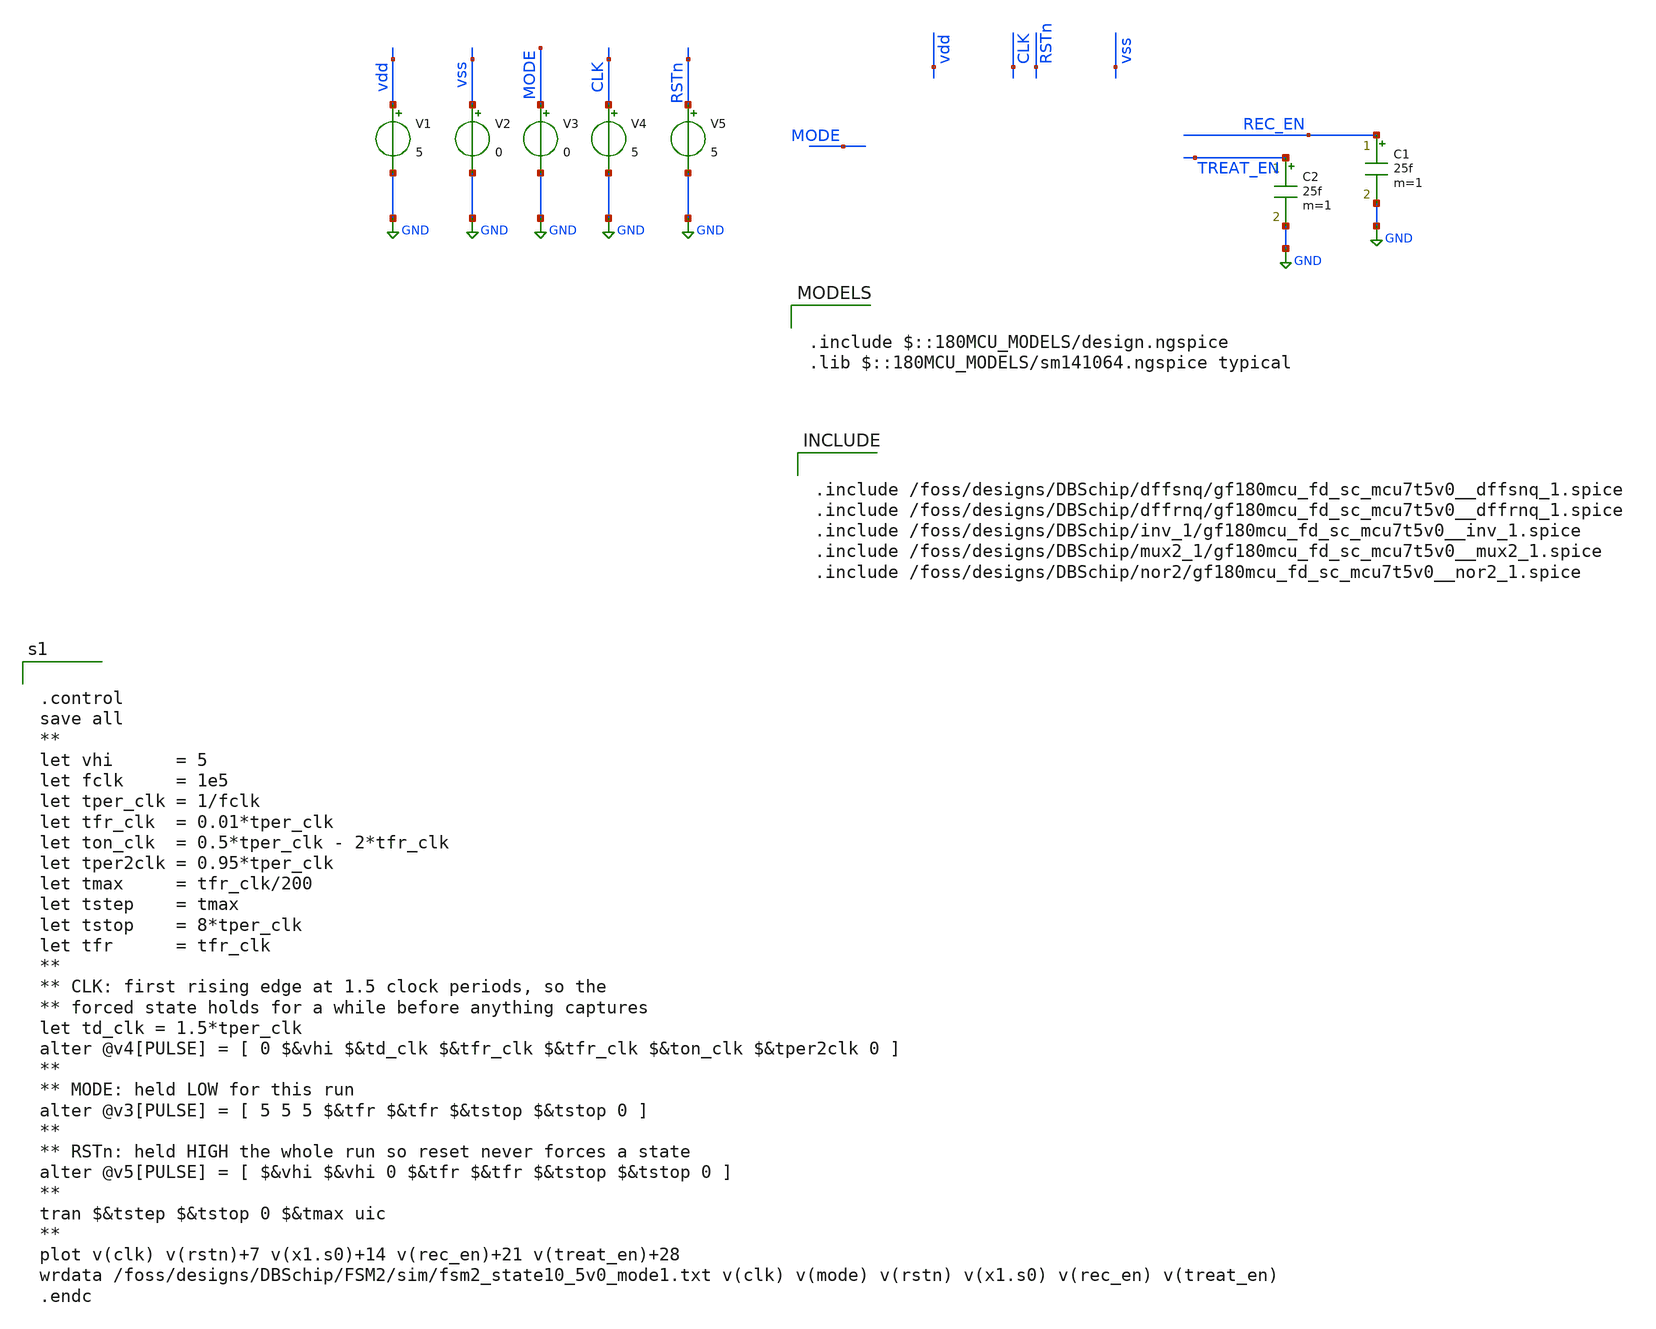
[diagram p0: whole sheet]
** sch_path: FSM2/FSM2_tb_postPEX.sch
**.subckt FSM2_tb_postPEX
V1 vdd GND 5
V2 vss GND 0
V3 MODE GND 0
V4 CLK GND 5
V5 RSTn GND 5
C1 REC_EN GND 25f m=1
C2 TREAT_EN GND 25f m=1
**** begin user architecture code

.include $::180MCU_MODELS/design.ngspice
.lib $::180MCU_MODELS/sm141064.ngspice typical



.include /foss/designs/DBSchip/dffsnq/gf180mcu_fd_sc_mcu7t5v0__dffsnq_1.spice
.include /foss/designs/DBSchip/dffrnq/gf180mcu_fd_sc_mcu7t5v0__dffrnq_1.spice
.include /foss/designs/DBSchip/inv_1/gf180mcu_fd_sc_mcu7t5v0__inv_1.spice
.include /foss/designs/DBSchip/mux2_1/gf180mcu_fd_sc_mcu7t5v0__mux2_1.spice
.include /foss/designs/DBSchip/nor2/gf180mcu_fd_sc_mcu7t5v0__nor2_1.spice




* NGSPICE file created from FSM2.ext - technology: gf180mcuD

.subckt dffsnq SETN Q CLK VNW VPW a_1836_282# a_855_238# a_1492_238# a_3220_277# a_1179_653#
+  a_975_282# a_175_277# a_587_598# a_383_277# a_1432_653# a_2588_282# a_2364_282#  a_3268_233# a_383_598#
+ a_1423_282#
X0 a_975_282# a_855_238# a_383_598# VNW pfet_05v0 ad=0.1313p pd=1.025u as=0.22725p ps=1.91u w=0.505u
+ l=0.5u
X1 a_383_598# a_1492_238# a_1432_653# VNW pfet_05v0 ad=0.3975p pd=2.185u as=0.101p ps=0.905u
+ w=0.505u l=0.5u
X2 a_1836_282# a_1179_653# a_383_277# VPW nfet_05v0 ad=86.39999f pd=0.84u as=93.59999f ps=0.88u
+ w=0.36u l=0.6u
X3 a_587_598# a_175_277# a_383_598# VNW pfet_05v0 ad=0.3806p pd=2.61u as=0.2249p ps=1.385u w=0.865u
+ l=0.5u
X4 a_1432_653# a_175_277# a_1179_653# VNW pfet_05v0 ad=0.101p pd=0.905u as=0.19315p ps=1.27u
+ w=0.505u l=0.5u
X5 a_2364_282# a_175_277# a_1492_238# VNW pfet_05v0 ad=0.1079p pd=0.935u as=0.27805p ps=2.17u
+ w=0.415u l=0.5u
X6 a_2588_282# SETN a_383_598# VNW pfet_05v0 ad=0.2028p pd=1.3u as=0.3432p ps=2.44u w=0.78u l=0.5u
X7 a_1179_653# a_175_277# a_975_282# VPW nfet_05v0 ad=93.59999f pd=0.88u as=93.59999f ps=0.88u
+ w=0.36u l=0.6u
X8 a_383_277# a_3268_233# a_3220_277# VPW nfet_05v0 ad=0.14985p pd=1.145u as=48.6f ps=0.645u
+ w=0.405u l=0.6u
X9 a_383_277# a_1492_238# a_1423_282# VPW nfet_05v0 ad=93.59999f pd=0.88u as=62.1f ps=0.705u w=0.36u
+ l=0.6u
X10 a_2364_282# a_587_598# a_1492_238# VPW nfet_05v0 ad=93.59999f pd=0.88u as=0.1989p ps=1.465u
+ w=0.36u l=0.6u
X11 a_1179_653# a_587_598# a_975_282# VNW pfet_05v0 ad=0.19315p pd=1.27u as=0.1313p ps=1.025u
+ w=0.505u l=0.5u
X12 a_587_598# a_175_277# a_383_277# VPW nfet_05v0 ad=0.1782p pd=1.69u as=0.1053p ps=0.925u w=0.405u
+ l=0.6u
X13 a_1492_238# SETN a_1836_282# VPW nfet_05v0 ad=0.1989p pd=1.465u as=86.39999f ps=0.84u w=0.36u
+ l=0.6u
X14 a_2588_282# a_587_598# a_2364_282# VNW pfet_05v0 ad=0.1826p pd=1.71u as=0.1079p ps=0.935u
+ w=0.415u l=0.5u
X15 a_383_598# a_3268_233# a_2588_282# VNW pfet_05v0 ad=0.3276p pd=1.62u as=0.2028p ps=1.3u w=0.78u
+ l=0.5u
X16 a_975_282# a_855_238# a_383_277# VPW nfet_05v0 ad=93.59999f pd=0.88u as=0.1584p ps=1.6u w=0.36u
+ l=0.6u
X17 a_3220_277# SETN a_2588_282# VPW nfet_05v0 ad=48.6f pd=0.645u as=0.3123p ps=2.38u w=0.405u
+ l=0.6u
X18 a_383_277# CLK a_175_277# VPW nfet_05v0 ad=0.1053p pd=0.925u as=0.1782p ps=1.69u w=0.405u l=0.6u
X19 a_3268_233# a_2364_282# a_383_277# VPW nfet_05v0 ad=0.1782p pd=1.69u as=0.14985p ps=1.145u
+ w=0.405u l=0.6u
X20 Q a_3268_233# a_383_598# VNW pfet_05v0 ad=0.6561p pd=3.51u as=0.5346p ps=3.31u w=1.215u l=0.5u
X21 a_383_598# SETN a_1492_238# VNW pfet_05v0 ad=0.4149p pd=2.65u as=0.1521p ps=1.105u w=0.585u
+ l=0.5u
X22 a_2588_282# a_175_277# a_2364_282# VPW nfet_05v0 ad=0.2898p pd=2.33u as=93.59999f ps=0.88u
+ w=0.36u l=0.6u
X23 a_3268_233# a_2364_282# a_383_598# VNW pfet_05v0 ad=0.3432p pd=2.44u as=0.3276p ps=1.62u w=0.78u
+ l=0.5u
X24 a_1492_238# a_1179_653# a_383_598# VNW pfet_05v0 ad=0.1521p pd=1.105u as=0.3975p ps=2.185u
+ w=0.585u l=0.5u
X25 Q a_3268_233# a_383_277# VPW nfet_05v0 ad=0.3586p pd=2.51u as=0.3586p ps=2.51u w=0.815u l=0.6u
X26 a_383_598# CLK a_175_277# VNW pfet_05v0 ad=0.2249p pd=1.385u as=0.3806p ps=2.61u w=0.865u l=0.5u
X27 a_1423_282# a_587_598# a_1179_653# VPW nfet_05v0 ad=62.1f pd=0.705u as=93.59999f ps=0.88u
+ w=0.36u l=0.6u
C0 a_383_277# a_175_277# 0.28633f
C1 a_1432_653# a_1179_653# 0.00215f
C2 SETN VNW 0.81105f
C3 a_975_282# a_175_277# 0.0157f
C4 a_3220_277# a_2364_282# 0.00413f
C5 a_383_277# a_383_598# 0.01381f
C6 a_1432_653# a_1492_238# 0
C7 SETN a_3268_233# 0.08929f
C8 a_1179_653# a_175_277# 0.20639f
C9 a_1179_653# a_383_598# 0.03968f
C10 a_175_277# a_1492_238# 0.84088f
C11 a_383_277# a_975_282# 0.05001f
C12 a_1836_282# a_1492_238# 0.00275f
C13 a_383_598# a_1492_238# 0.01626f
C14 Q a_175_277# 0
C15 a_383_277# a_1179_653# 0.06022f
C16 a_975_282# a_1179_653# 0.06821f
C17 Q a_383_598# 0.28218f
C18 a_587_598# a_855_238# 0.4001f
C19 a_383_277# a_1492_238# 0.02735f
C20 a_2588_282# a_587_598# 0.05668f
C21 VNW a_855_238# 0.1615f
C22 VNW a_2588_282# 0.04382f
C23 a_383_277# Q 0.13127f
C24 a_1423_282# a_587_598# 0.00269f
C25 VNW a_587_598# 0.40096f
C26 a_1179_653# a_1492_238# 0.38742f
C27 a_3268_233# a_2588_282# 0.00955f
C28 a_2364_282# a_175_277# 0.15368f
C29 a_3268_233# a_587_598# 0
C30 a_2364_282# a_383_598# 0.07341f
C31 a_3220_277# a_2588_282# 0.0012f
C32 a_3268_233# VNW 0.32346f
C33 SETN a_175_277# 0.07777f
C34 a_383_277# a_2364_282# 1.18908f
C35 SETN a_383_598# 0.12782f
C36 SETN a_383_277# 0.00808f
C37 a_2364_282# a_1492_238# 0.15287f
C38 CLK a_587_598# 0.00131f
C39 a_2364_282# Q 0
C40 CLK VNW 0.13659f
C41 SETN a_1179_653# 0.06324f
C42 SETN a_1492_238# 0.07298f
C43 a_175_277# a_855_238# 0.0927f
C44 a_2588_282# a_175_277# 0.00597f
C45 a_383_598# a_855_238# 0.00494f
C46 a_175_277# a_587_598# 0.47313f
C47 a_2588_282# a_383_598# 0.20863f
C48 a_1836_282# a_587_598# 0.00762f
C49 VNW a_175_277# 0.90944f
C50 a_383_598# a_587_598# 0.62458f
C51 a_383_277# a_855_238# 0.06788f
C52 a_975_282# a_855_238# 0.1081f
C53 VNW a_383_598# 0.5391f
C54 a_3268_233# a_175_277# 0
C55 a_383_277# a_587_598# 1.07431f
C56 a_383_277# a_1423_282# 0.00364f
C57 a_975_282# a_587_598# 0.42776f
C58 a_1179_653# a_855_238# 0
C59 a_3268_233# a_383_598# 0.35131f
C60 a_383_277# VNW 0.00946f
C61 SETN a_2364_282# 0.0706f
C62 a_975_282# VNW 0.01368f
C63 a_3220_277# a_383_598# 0
C64 a_1179_653# a_587_598# 0.86961f
C65 a_2588_282# a_1492_238# 0
C66 a_1179_653# a_1423_282# 0
C67 a_383_277# a_3268_233# 0.13677f
C68 a_1179_653# VNW 0.22386f
C69 a_587_598# a_1492_238# 0.31725f
C70 VNW a_1492_238# 0.21951f
C71 Q a_587_598# 0
C72 Q VNW 0.03162f
C73 CLK a_175_277# 0.70097f
C74 CLK a_383_598# 0.02209f
C75 a_3268_233# Q 0.17947f
C76 a_1432_653# a_175_277# 0.00838f
C77 a_2364_282# a_2588_282# 0.56917f
C78 a_383_277# CLK 0.02194f
C79 a_2364_282# a_587_598# 0.154f
C80 a_2364_282# VNW 0.20903f
C81 a_383_598# a_175_277# 1.41468f
C82 SETN a_2588_282# 0.30222f
C83 a_3268_233# a_2364_282# 0.51404f
C84 SETN a_587_598# 0.0839f
C85 Q VPW 0.10557f
C86 SETN VPW 0.71025f
C87 CLK VPW 0.29047f
C88 VNW VPW 6.44257f
C89 a_2588_282# VPW 0.04999f
C90 a_383_277# VPW 1.35707f
C91 a_2364_282# VPW 0.43408f
C92 a_3268_233# VPW 0.58406f
C93 a_975_282# VPW 0.01977f
C94 a_1179_653# VPW 0.30208f
C95 a_1492_238# VPW 0.28651f
C96 a_855_238# VPW 0.2471f
C97 a_587_598# VPW 1.21246f
C98 a_383_598# VPW 0.83318f
C99 a_175_277# VPW 1.31409f
.ends

.subckt or2 MODE A1 VNW VPW a_n505_n1653# a_159_n1784# a_n525_n2163# a_n317_n1653#  a_n113_n1653#
X0 a_159_n1784# a_n505_n1653# a_n113_n1653# VNW pfet_05v0 ad=0.5368p pd=3.32u as=0.38705p ps=2.08u
+ w=1.22u l=0.5u
X1 a_n317_n1653# A1 a_n505_n1653# VNW pfet_05v0 ad=0.1469p pd=1.085u as=0.2486p ps=2.01u w=0.565u
+ l=0.5u
X2 a_159_n1784# a_n505_n1653# a_n525_n2163# VPW nfet_05v0 ad=0.3608p pd=2.52u as=0.2288p ps=1.58u
+ w=0.82u l=0.6u
X3 a_n113_n1653# MODE a_n317_n1653# VNW pfet_05v0 ad=0.38705p pd=2.08u as=0.1469p ps=1.085u w=0.565u
+ l=0.5u
X4 a_n525_n2163# MODE a_n505_n1653# VPW nfet_05v0 ad=0.2288p pd=1.58u as=93.59999f ps=0.88u w=0.36u
+ l=0.6u
X5 a_n505_n1653# A1 a_n525_n2163# VPW nfet_05v0 ad=93.59999f pd=0.88u as=0.1584p ps=1.6u w=0.36u
+ l=0.6u
C0 a_n525_n2163# VNW 0.01004f
C1 a_n317_n1653# a_n113_n1653# 0.00536f
C2 VNW MODE 0.21631f
C3 a_n505_n1653# VNW 0.15724f
C4 a_n525_n2163# a_n113_n1653# 0.00865f
C5 a_n113_n1653# MODE 0.14763f
C6 a_n505_n1653# a_n113_n1653# 0.30704f
C7 a_n525_n2163# A1 0.05074f
C8 a_n525_n2163# a_159_n1784# 0.15826f
C9 VNW a_n113_n1653# 0.11771f
C10 a_n317_n1653# a_n525_n2163# 0
C11 A1 MODE 0.0624f
C12 a_159_n1784# MODE 0.0276f
C13 a_n505_n1653# A1 0.54089f
C14 a_n505_n1653# a_159_n1784# 0.18159f
C15 a_n317_n1653# MODE 0.00196f
C16 a_n317_n1653# a_n505_n1653# 0.00762f
C17 VNW A1 0.22f
C18 VNW a_159_n1784# 0.03388f
C19 a_n525_n2163# MODE 0.02575f
C20 a_n525_n2163# a_n505_n1653# 0.25049f
C21 a_n505_n1653# MODE 0.50537f
C22 a_n113_n1653# A1 0.01431f
C23 a_n113_n1653# a_159_n1784# 0.19605f
C24 MODE VPW 0.31344f
C25 A1 VPW 0.39469f
C26 VNW VPW 1.65967f
C27 a_n525_n2163# VPW 0.35972f
C28 a_159_n1784# VPW 0.10275f
C29 a_n113_n1653# VPW 0.23302f
C30 a_n505_n1653# VPW 0.34568f
.ends

.subckt nor2 REC_EN TREAT_EN A2 VSS VDD w_1180_n1958# a_1490_n1804# VSUBS
X0 a_1490_n1804# REC_EN VDD w_1180_n1958# pfet_05v0 ad=0.4087p pd=1.89u as=0.5368p ps=3.32u w=1.22u
+ l=0.5u
X1 TREAT_EN REC_EN VSS VSUBS nfet_05v0 ad=0.1469p pd=1.085u as=0.2486p ps=2.01u w=0.565u l=0.6u
X2 TREAT_EN A2 a_1490_n1804# w_1180_n1958# pfet_05v0 ad=0.5368p pd=3.32u as=0.4087p ps=1.89u w=1.22u
+ l=0.5u
X3 VSS A2 TREAT_EN VSUBS nfet_05v0 ad=0.2486p pd=2.01u as=0.1469p ps=1.085u w=0.565u l=0.6u
C0 TREAT_EN w_1180_n1958# 0.01978f
C1 A2 w_1180_n1958# 0.13314f
C2 w_1180_n1958# REC_EN 0.1288f
C3 TREAT_EN A2 0.57853f
C4 VDD w_1180_n1958# 0.09421f
C5 TREAT_EN REC_EN 0.37841f
C6 A2 REC_EN 0.03781f
C7 TREAT_EN VDD 0.11792f
C8 A2 VDD 0.0227f
C9 VSS a_1490_n1804# 0
C10 VDD REC_EN 0.25532f
C11 VSS w_1180_n1958# 0.01214f
C12 TREAT_EN a_1490_n1804# 0.02369f
C13 TREAT_EN VSS 0.08738f
C14 A2 VSS 0.16225f
C15 a_1490_n1804# REC_EN 0.00898f
C16 VDD a_1490_n1804# 0.01396f
C17 VSS REC_EN 0.04452f
C18 VSS VDD 0.02591f
C19 VDD VSUBS 0.21903f
C20 TREAT_EN VSUBS 0.05889f
C21 VSS VSUBS 0.3776f
C22 A2 VSUBS 0.32864f
C23 REC_EN VSUBS 0.33451f
C24 w_1180_n1958# VSUBS 1.31158f
.ends

.subckt dffrnq RN Q CLK VNW VPW a_1002_n2102# a_1458_n1702# a_2250_n1702# a_2667_n1842#  a_38_n1706#
+ a_798_n2102# a_698_n2146# a_450_n2119# a_1310_n2146# a_246_n2119# a_246_n1706#  a_1206_n2102# a_1290_n1702#
+ a_2562_n1702# a_3043_n1702#
X0 a_246_n1706# RN a_1458_n1702# VPW nfet_05v0 ad=0.2016p pd=1.48u as=43.2f ps=0.6u w=0.36u l=0.6u
X1 a_3043_n1702# RN a_246_n1706# VPW nfet_05v0 ad=0.134p pd=1.1u as=0.1224p ps=1.04u w=0.36u l=0.6u
X2 a_2562_n1702# a_450_n2119# a_2250_n1702# VNW pfet_05v0 ad=0.1313p pd=1.025u as=0.25375p ps=1.51u
+ w=0.505u l=0.5u
X3 a_798_n2102# a_698_n2146# a_246_n2119# VNW pfet_05v0 ad=0.2028p pd=1.3u as=0.3432p ps=2.44u
+ w=0.78u l=0.5u
X4 a_246_n1706# a_2667_n1842# a_2562_n1702# VPW nfet_05v0 ad=0.1224p pd=1.04u as=94.5f ps=0.885u
+ w=0.36u l=0.6u
X5 a_450_n2119# a_38_n1706# a_246_n1706# VPW nfet_05v0 ad=0.1782p pd=1.69u as=0.1053p ps=0.925u
+ w=0.405u l=0.6u
X6 a_1206_n2102# a_38_n1706# a_1002_n2102# VNW pfet_05v0 ad=0.2028p pd=1.3u as=0.2028p ps=1.3u
+ w=0.78u l=0.5u
X7 a_2667_n1842# a_2250_n1702# a_3043_n1702# VPW nfet_05v0 ad=0.176p pd=1.68u as=0.134p ps=1.1u
+ w=0.4u l=0.6u
X8 a_1206_n2102# RN a_246_n2119# VNW pfet_05v0 ad=0.3432p pd=2.44u as=0.45p ps=2.02u w=0.78u l=0.5u
X9 a_2562_n1702# a_38_n1706# a_2250_n1702# VPW nfet_05v0 ad=94.5f pd=0.885u as=0.2007p ps=1.475u
+ w=0.36u l=0.6u
X10 a_246_n1706# CLK a_38_n1706# VPW nfet_05v0 ad=0.1053p pd=0.925u as=0.1782p ps=1.69u w=0.405u
+ l=0.6u
X11 a_1310_n2146# a_1002_n2102# a_246_n2119# VNW pfet_05v0 ad=0.2424p pd=1.465u as=0.2222p ps=1.89u
+ w=0.505u l=0.5u
X12 a_2667_n1842# RN a_246_n2119# VNW pfet_05v0 ad=0.26p pd=1.52u as=0.29465p ps=1.74u w=1u l=0.5u
X13 a_2250_n1702# a_450_n2119# a_1310_n2146# VPW nfet_05v0 ad=0.2007p pd=1.475u as=0.2007p ps=1.475u
+ w=0.36u l=0.6u
X14 a_246_n2119# CLK a_38_n1706# VNW pfet_05v0 ad=0.2249p pd=1.385u as=0.3806p ps=2.61u w=0.865u
+ l=0.5u
X15 a_246_n2119# a_2667_n1842# a_2562_n1702# VNW pfet_05v0 ad=0.29465p pd=1.74u as=0.1313p ps=1.025u
+ w=0.505u l=0.5u
X16 a_1290_n1702# a_450_n2119# a_1002_n2102# VPW nfet_05v0 ad=43.2f pd=0.6u as=93.59999f ps=0.88u
+ w=0.36u l=0.6u
X17 Q a_2667_n1842# a_246_n2119# VNW pfet_05v0 ad=0.63787p pd=3.48u as=0.5346p ps=3.31u w=1.215u
+ l=0.5u
X18 a_246_n2119# a_1310_n2146# a_1206_n2102# VNW pfet_05v0 ad=0.45p pd=2.02u as=0.2028p ps=1.3u
+ w=0.78u l=0.5u
X19 Q a_2667_n1842# a_246_n1706# VPW nfet_05v0 ad=0.42787p pd=2.68u as=0.3586p ps=2.51u w=0.815u
+ l=0.6u
X20 a_798_n2102# a_698_n2146# a_246_n1706# VPW nfet_05v0 ad=93.59999f pd=0.88u as=0.1584p ps=1.6u
+ w=0.36u l=0.6u
X21 a_2250_n1702# a_38_n1706# a_1310_n2146# VNW pfet_05v0 ad=0.25375p pd=1.51u as=0.2424p ps=1.465u
+ w=0.505u l=0.5u
X22 a_246_n2119# a_2250_n1702# a_2667_n1842# VNW pfet_05v0 ad=0.44p pd=2.88u as=0.26p ps=1.52u w=1u
+ l=0.5u
X23 a_1002_n2102# a_38_n1706# a_798_n2102# VPW nfet_05v0 ad=93.59999f pd=0.88u as=93.59999f ps=0.88u
+ w=0.36u l=0.6u
X24 a_450_n2119# a_38_n1706# a_246_n2119# VNW pfet_05v0 ad=0.3806p pd=2.61u as=0.2249p ps=1.385u
+ w=0.865u l=0.5u
X25 a_1002_n2102# a_450_n2119# a_798_n2102# VNW pfet_05v0 ad=0.2028p pd=1.3u as=0.2028p ps=1.3u
+ w=0.78u l=0.5u
X26 a_1458_n1702# a_1310_n2146# a_1290_n1702# VPW nfet_05v0 ad=43.2f pd=0.6u as=43.2f ps=0.6u
+ w=0.36u l=0.6u
X27 a_1310_n2146# a_1002_n2102# a_246_n1706# VPW nfet_05v0 ad=0.2007p pd=1.475u as=0.2016p ps=1.48u
+ w=0.36u l=0.6u
C0 a_38_n1706# a_2667_n1842# 0.01904f
C1 RN a_246_n2119# 0.03498f
C2 a_246_n1706# Q 0.11398f
C3 a_1002_n2102# a_798_n2102# 0.04844f
C4 a_2562_n1702# a_2667_n1842# 0.11606f
C5 a_1310_n2146# a_246_n2119# 0.09419f
C6 a_38_n1706# a_450_n2119# 0.53697f
C7 a_2562_n1702# a_450_n2119# 0.27749f
C8 VNW CLK 0.13704f
C9 a_1002_n2102# a_246_n2119# 0.11921f
C10 a_1002_n2102# a_1290_n1702# 0
C11 a_2667_n1842# a_3043_n1702# 0.00177f
C12 a_38_n1706# a_2562_n1702# 0.00367f
C13 a_1002_n2102# a_698_n2146# 0
C14 VNW Q 0.03166f
C15 a_246_n1706# a_2667_n1842# 0.18639f
C16 RN Q 0
C17 a_450_n2119# a_246_n1706# 1.20327f
C18 a_450_n2119# a_1206_n2102# 0.009f
C19 a_38_n1706# a_246_n1706# 0.29961f
C20 a_2562_n1702# a_246_n1706# 0.1285f
C21 VNW a_2667_n1842# 0.35472f
C22 a_450_n2119# VNW 0.34128f
C23 a_38_n1706# a_1206_n2102# 0.007f
C24 RN a_2667_n1842# 0.33647f
C25 a_246_n2119# a_2250_n1702# 1.11667f
C26 a_450_n2119# RN 0.07873f
C27 a_246_n2119# a_798_n2102# 0
C28 a_450_n2119# a_1310_n2146# 0.8821f
C29 a_38_n1706# VNW 1.28833f
C30 a_2562_n1702# VNW 0.02016f
C31 a_698_n2146# a_798_n2102# 0.08286f
C32 a_1002_n2102# a_450_n2119# 0.36196f
C33 a_38_n1706# RN 0.0801f
C34 a_38_n1706# a_1310_n2146# 0.05539f
C35 a_2562_n1702# RN 0.03878f
C36 a_698_n2146# a_246_n2119# 0.00937f
C37 a_1002_n2102# a_38_n1706# 0.08126f
C38 Q a_2250_n1702# 0.01436f
C39 VNW a_246_n1706# 0.0106f
C40 RN a_3043_n1702# 0.01068f
C41 CLK a_246_n2119# 0.02303f
C42 VNW a_1206_n2102# 0.01627f
C43 RN a_246_n1706# 0.45994f
C44 Q a_246_n2119# 0.1499f
C45 a_246_n1706# a_1310_n2146# 0.01482f
C46 RN a_1206_n2102# 0.02104f
C47 a_1002_n2102# a_246_n1706# 0.04356f
C48 a_1206_n2102# a_1310_n2146# 0.02667f
C49 a_2667_n1842# a_2250_n1702# 0.63332f
C50 a_450_n2119# a_2250_n1702# 0.51037f
C51 a_450_n2119# a_1458_n1702# 0.00227f
C52 RN VNW 0.32949f
C53 a_1002_n2102# a_1206_n2102# 0.66083f
C54 VNW a_1310_n2146# 0.14901f
C55 a_450_n2119# a_798_n2102# 0.40164f
C56 a_246_n2119# a_2667_n1842# 0.10205f
C57 a_38_n1706# a_2250_n1702# 0.0428f
C58 a_1002_n2102# VNW 0.24136f
C59 RN a_1310_n2146# 0.07929f
C60 a_450_n2119# a_246_n2119# 0.45627f
C61 a_1290_n1702# a_450_n2119# 0.00207f
C62 a_2562_n1702# a_2250_n1702# 0.11969f
C63 a_38_n1706# a_798_n2102# 0.01185f
C64 a_698_n2146# a_450_n2119# 0.32879f
C65 a_1002_n2102# RN 0.0832f
C66 a_1002_n2102# a_1310_n2146# 0.93419f
C67 a_38_n1706# a_246_n2119# 0.41709f
C68 a_2562_n1702# a_246_n2119# 0.00217f
C69 a_450_n2119# CLK 0.00276f
C70 a_698_n2146# a_38_n1706# 0.09411f
C71 a_246_n1706# a_2250_n1702# 0.03193f
C72 Q a_2667_n1842# 0.10944f
C73 a_246_n1706# a_1458_n1702# 0.0019f
C74 a_246_n1706# a_798_n2102# 0.05215f
C75 a_38_n1706# CLK 0.6696f
C76 a_1290_n1702# a_246_n1706# 0.0017f
C77 a_246_n1706# a_246_n2119# 0.01338f
C78 a_38_n1706# Q 0
C79 VNW a_2250_n1702# 0.21243f
C80 a_698_n2146# a_246_n1706# 0.06462f
C81 a_1206_n2102# a_246_n2119# 0.28263f
C82 VNW a_798_n2102# 0.01023f
C83 RN a_2250_n1702# 0.09434f
C84 a_450_n2119# a_2667_n1842# 0.02046f
C85 a_1310_n2146# a_2250_n1702# 0.05672f
C86 a_246_n1706# CLK 0.02288f
C87 VNW a_246_n2119# 0.50314f
C88 a_1002_n2102# a_2250_n1702# 0.00123f
C89 a_698_n2146# VNW 0.12823f
C90 a_1002_n2102# a_1458_n1702# 0
C91 Q VPW 0.11299f
C92 RN VPW 1.36673f
C93 CLK VPW 0.29124f
C94 VNW VPW 6.1377f
C95 a_1206_n2102# VPW 0.01297f
C96 a_246_n2119# VPW 0.79945f
C97 a_2562_n1702# VPW 0.01697f
C98 a_2250_n1702# VPW 0.37166f
C99 a_2667_n1842# VPW 0.62251f
C100 a_1002_n2102# VPW 0.29173f
C101 a_798_n2102# VPW 0.02321f
C102 a_1310_n2146# VPW 0.27904f
C103 a_698_n2146# VPW 0.25341f
C104 a_450_n2119# VPW 0.68441f
C105 a_246_n1706# VPW 1.42701f
C106 a_38_n1706# VPW 1.43589f
.ends

.subckt and2 A1 VNW VPW a_3638_891# a_3366_452# a_3758_935# a_3366_935# a_3574_935#  a_4026_452#
X0 a_4026_452# a_3366_935# a_3366_452# VNW pfet_05v0 ad=0.5346p pd=3.31u as=0.40575p ps=2.055u
+ w=1.215u l=0.5u
X1 a_3758_935# a_3638_891# a_3574_935# VPW nfet_05v0 ad=0.23405p pd=1.555u as=58.39999f ps=0.685u
+ w=0.365u l=0.6u
X2 a_3366_935# A1 a_3366_452# VNW pfet_05v0 ad=0.156p pd=1.12u as=0.264p ps=2.08u w=0.6u l=0.5u
X3 a_3574_935# A1 a_3366_935# VPW nfet_05v0 ad=58.39999f pd=0.685u as=0.1606p ps=1.61u w=0.365u
+ l=0.6u
X4 a_3366_452# a_3638_891# a_3366_935# VNW pfet_05v0 ad=0.40575p pd=2.055u as=0.156p ps=1.12u w=0.6u
+ l=0.5u
X5 a_4026_452# a_3366_935# a_3758_935# VPW nfet_05v0 ad=0.3586p pd=2.51u as=0.23405p ps=1.555u
+ w=0.815u l=0.6u
C0 a_3366_452# a_3366_935# 0.13019f
C1 a_3758_935# a_4026_452# 0.10282f
C2 a_3366_452# a_3638_891# 0.18402f
C3 a_3574_935# a_4026_452# 0
C4 a_3366_452# a_4026_452# 0.15821f
C5 VNW a_3758_935# 0.00793f
C6 a_3366_935# A1 0.37712f
C7 a_3638_891# A1 0.06143f
C8 VNW a_3366_452# 0.12561f
C9 a_4026_452# A1 0
C10 a_3638_891# a_3366_935# 0.47278f
C11 a_4026_452# a_3366_935# 0.21527f
C12 a_3574_935# a_3758_935# 0.00145f
C13 a_4026_452# a_3638_891# 0.02017f
C14 a_3366_452# a_3758_935# 0.01413f
C15 VNW A1 0.20677f
C16 VNW a_3366_935# 0.1625f
C17 VNW a_3638_891# 0.20463f
C18 VNW a_4026_452# 0.03284f
C19 a_3758_935# A1 0.01116f
C20 a_3758_935# a_3366_935# 0.24575f
C21 a_3574_935# a_3366_935# 0.00334f
C22 a_3758_935# a_3638_891# 0.01199f
C23 a_3366_452# A1 0.04397f
C24 A1 VPW 0.32127f
C25 VNW VPW 1.65967f
C26 a_3366_452# VPW 0.25125f
C27 a_4026_452# VPW 0.09648f
C28 a_3638_891# VPW 0.26226f
C29 a_3758_935# VPW 0.40776f
C30 a_3366_935# VPW 0.37412f
.ends

.subckt FSM2 MODE RSTn VSS CLK VDD TREAT_EN REC_EN
Xdffsnq_0 RSTn S0 CLK VDD VSS dffsnq_0/a_1836_282#  m2_3305_n910# dffsnq_0/a_1492_238#
+ dffsnq_0/a_3220_277# dffsnq_0/a_1179_653# dffsnq_0/a_975_282#  dffsnq_0/a_175_277# dffsnq_0/a_587_598# VSS
+ dffsnq_0/a_1432_653# dffsnq_0/a_2588_282#  dffsnq_0/a_2364_282# dffsnq_0/a_3268_233# VDD dffsnq_0/a_1423_282# dffsnq
Xor2_0 MODE REC_EN VDD VSS or2_0/a_n505_n1653# m2_3305_n910# VSS  or2_0/a_n317_n1653# VDD or2
Xnor2_0 REC_EN TREAT_EN S0 VSS VDD VDD nor2_0/a_1490_n1804#  VSS nor2
Xdffrnq_0 RSTn REC_EN CLK VDD VSS dffrnq_0/a_1002_n2102#  dffrnq_0/a_1458_n1702#
+ dffrnq_0/a_2250_n1702# dffrnq_0/a_2667_n1842# dffrnq_0/a_38_n1706#  dffrnq_0/a_798_n2102# m2_3239_n1773#
+ dffrnq_0/a_450_n2119# dffrnq_0/a_1310_n2146#  VDD VSS dffrnq_0/a_1206_n2102# dffrnq_0/a_1290_n1702#
+ dffrnq_0/a_2562_n1702#  dffrnq_0/a_3043_n1702# dffrnq
Xand2_0 S0 VDD VSS MODE VDD VSS and2_0/a_3366_935#  and2_0/a_3574_935# m2_3239_n1773# and2
C0 dffsnq_0/a_2364_282# VDD 0.00239f
C1 REC_EN TREAT_EN 0.03989f
C2 S0 dffrnq_0/a_798_n2102# 0.02803f
C3 S0 RSTn 0.03746f
C4 dffsnq_0/a_3220_277# REC_EN 0
C5 MODE m2_3305_n910# 0.00194f
C6 or2_0/a_n505_n1653# REC_EN 0.03149f
C7 S0 dffrnq_0/a_2562_n1702# 0.0365f
C8 dffrnq_0/a_38_n1706# m2_3239_n1773# 0.13668f
C9 S0 and2_0/a_3574_935# 0
C10 S0 dffrnq_0/a_1290_n1702# 0
C11 dffsnq_0/a_587_598# m2_3305_n910# 0.03797f
C12 dffrnq_0/a_2250_n1702# REC_EN 0.02201f
C13 S0 VDD 0.48506f
C14 S0 dffsnq_0/a_3268_233# 0.0078f
C15 dffsnq_0/a_2364_282# REC_EN 0.01621f
C16 MODE m2_3239_n1773# 0.00154f
C17 or2_0/a_n505_n1653# m2_3305_n910# 0.00284f
C18 dffrnq_0/a_1002_n2102# VDD 0
C19 dffsnq_0/a_1492_238# RSTn 0
C20 m2_3239_n1773# TREAT_EN 0
C21 dffrnq_0/a_38_n1706# CLK 0.01222f
C22 or2_0/a_n505_n1653# m2_3239_n1773# 0.00108f
C23 dffsnq_0/a_175_277# CLK 0.01222f
C24 dffsnq_0/a_2364_282# dffrnq_0/a_2667_n1842# 0
C25 S0 REC_EN 0.80131f
C26 dffrnq_0/a_798_n2102# dffrnq_0/a_450_n2119# -0.01121f
C27 REC_EN dffrnq_0/a_1002_n2102# 0.01893f
C28 MODE CLK 0.00675f
C29 dffsnq_0/a_1492_238# VDD 0
C30 dffsnq_0/a_2588_282# RSTn 0
C31 and2_0/a_3366_935# VDD -0.00943f
C32 S0 dffrnq_0/a_2667_n1842# 0.11643f
C33 CLK TREAT_EN 0
C34 dffrnq_0/a_38_n1706# dffsnq_0/a_1179_653# 0
C35 dffrnq_0/a_450_n2119# VDD -0
C36 or2_0/a_n505_n1653# CLK 0.01188f
C37 dffrnq_0/a_1310_n2146# VDD 0
C38 dffrnq_0/a_38_n1706# dffsnq_0/a_175_277# 0.03768f
C39 dffsnq_0/a_1492_238# REC_EN 0.01008f
C40 S0 m2_3239_n1773# 0.45662f
C41 dffsnq_0/a_2588_282# VDD -0
C42 MODE dffsnq_0/a_1179_653# 0
C43 dffsnq_0/a_1836_282# REC_EN 0
C44 m2_3239_n1773# dffrnq_0/a_1002_n2102# 0
C45 MODE dffrnq_0/a_38_n1706# 0
C46 REC_EN and2_0/a_3366_935# 0.06825f
C47 MODE dffsnq_0/a_175_277# 0
C48 dffsnq_0/a_587_598# dffrnq_0/a_38_n1706# 0
C49 dffrnq_0/a_450_n2119# REC_EN 0.16798f
C50 dffsnq_0/a_587_598# dffsnq_0/a_175_277# -0
C51 dffsnq_0/a_1492_238# m2_3305_n910# 0
C52 REC_EN dffrnq_0/a_1310_n2146# 0.03455f
C53 dffsnq_0/a_2588_282# REC_EN 0.00622f
C54 dffsnq_0/a_587_598# MODE 0
C55 nor2_0/a_1490_n1804# VDD 0
C56 dffsnq_0/a_975_282# VDD -0
C57 or2_0/a_n505_n1653# dffsnq_0/a_175_277# 0.00156f
C58 S0 CLK 0.0401f
C59 RSTn VDD 0.00464f
C60 dffrnq_0/a_798_n2102# VDD -0
C61 dffsnq_0/a_3268_233# RSTn 0
C62 dffrnq_0/a_2562_n1702# VDD -0
C63 or2_0/a_n505_n1653# MODE 0.00232f
C64 dffsnq_0/a_175_277# dffrnq_0/a_1206_n2102# 0
C65 m2_3239_n1773# and2_0/a_3366_935# 0.00515f
C66 m2_3239_n1773# dffrnq_0/a_450_n2119# 0.07464f
C67 nor2_0/a_1490_n1804# REC_EN 0.00313f
C68 REC_EN dffsnq_0/a_975_282# 0.00273f
C69 m2_3239_n1773# dffrnq_0/a_1310_n2146# 0
C70 dffsnq_0/a_3268_233# VDD 0.00814f
C71 dffrnq_0/a_798_n2102# REC_EN 0.01189f
C72 REC_EN RSTn 0.08278f
C73 dffsnq_0/a_1423_282# REC_EN 0
C74 S0 dffrnq_0/a_38_n1706# 0.0792f
C75 dffrnq_0/a_2562_n1702# REC_EN 0.02552f
C76 and2_0/a_3574_935# REC_EN 0.00105f
C77 dffrnq_0/a_1290_n1702# REC_EN 0
C78 S0 dffsnq_0/a_175_277# 0
C79 dffsnq_0/a_975_282# m2_3305_n910# 0.00259f
C80 CLK and2_0/a_3366_935# 0.01029f
C81 dffsnq_0/a_175_277# dffrnq_0/a_1002_n2102# 0
C82 S0 dffrnq_0/a_3043_n1702# 0
C83 S0 MODE 0.04189f
C84 RSTn m2_3305_n910# 0
C85 dffsnq_0/a_2364_282# dffrnq_0/a_2250_n1702# 0
C86 REC_EN VDD 0.22949f
C87 dffsnq_0/a_3268_233# REC_EN 0.00916f
C88 S0 dffrnq_0/a_1458_n1702# 0
C89 S0 dffsnq_0/a_587_598# 0
C90 MODE dffrnq_0/a_1002_n2102# 0
C91 dffsnq_0/a_587_598# dffrnq_0/a_1002_n2102# 0
C92 S0 TREAT_EN 0.02181f
C93 S0 dffsnq_0/a_3220_277# 0
C94 dffrnq_0/a_798_n2102# m2_3239_n1773# 0.02259f
C95 m2_3239_n1773# RSTn 0
C96 m2_3305_n910# VDD 0.06095f
C97 S0 or2_0/a_n505_n1653# 0
C98 dffrnq_0/a_38_n1706# dffsnq_0/a_1492_238# 0
C99 dffrnq_0/a_2667_n1842# VDD 0.00862f
C100 dffsnq_0/a_3268_233# dffrnq_0/a_2667_n1842# 0.0011f
C101 S0 dffrnq_0/a_2250_n1702# 0.10297f
C102 dffrnq_0/a_450_n2119# dffsnq_0/a_1179_653# 0
C103 or2_0/a_n317_n1653# VDD 0
C104 dffrnq_0/a_38_n1706# and2_0/a_3366_935# 0.00138f
C105 S0 dffrnq_0/a_1206_n2102# 0.03411f
C106 S0 dffsnq_0/a_2364_282# 0.00366f
C107 m2_3239_n1773# VDD 0.00785f
C108 dffrnq_0/a_1310_n2146# dffsnq_0/a_1179_653# 0
C109 dffsnq_0/a_1432_653# REC_EN 0
C110 dffsnq_0/a_175_277# dffrnq_0/a_450_n2119# 0
C111 REC_EN m2_3305_n910# 0.0677f
C112 dffsnq_0/a_175_277# dffrnq_0/a_1310_n2146# 0
C113 MODE and2_0/a_3366_935# 0.00751f
C114 dffrnq_0/a_2667_n1842# REC_EN 0.04664f
C115 MODE dffrnq_0/a_450_n2119# 0
C116 CLK RSTn 0.00159f
C117 dffsnq_0/a_587_598# dffrnq_0/a_450_n2119# 0.00481f
C118 or2_0/a_n317_n1653# REC_EN 0
C119 dffsnq_0/a_587_598# dffrnq_0/a_1310_n2146# 0
C120 TREAT_EN and2_0/a_3366_935# 0.0089f
C121 m2_3239_n1773# REC_EN 0.3421f
C122 or2_0/a_n505_n1653# and2_0/a_3366_935# 0.0036f
C123 S0 dffrnq_0/a_1002_n2102# 0.12522f
C124 dffsnq_0/a_1492_238# dffrnq_0/a_1206_n2102# 0
C125 CLK VDD 0.00924f
C126 m2_3239_n1773# m2_3305_n910# 0
C127 RSTn dffsnq_0/a_1179_653# 0.00638f
C128 dffsnq_0/a_175_277# RSTn 0.00151f
C129 MODE dffsnq_0/a_975_282# 0
C130 CLK REC_EN 0.01441f
C131 S0 dffsnq_0/a_1492_238# 0
C132 dffsnq_0/a_587_598# dffsnq_0/a_975_282# -0
C133 dffsnq_0/a_1179_653# VDD -0
C134 dffrnq_0/a_798_n2102# MODE 0
C135 dffsnq_0/a_1492_238# dffrnq_0/a_1002_n2102# 0
C136 dffrnq_0/a_38_n1706# VDD 0.00185f
C137 dffsnq_0/a_587_598# RSTn 0.04556f
C138 S0 and2_0/a_3366_935# 0.10792f
C139 dffsnq_0/a_175_277# VDD 0
C140 S0 dffrnq_0/a_450_n2119# 0.13606f
C141 CLK m2_3305_n910# 0.08319f
C142 S0 dffrnq_0/a_1310_n2146# 0.08139f
C143 MODE VDD 0.00701f
C144 S0 dffsnq_0/a_2588_282# 0
C145 dffsnq_0/a_587_598# VDD -0
C146 REC_EN dffsnq_0/a_1179_653# 0.00787f
C147 dffrnq_0/a_38_n1706# REC_EN 0.04348f
C148 CLK m2_3239_n1773# 0.04562f
C149 dffsnq_0/a_175_277# REC_EN 0.01819f
C150 TREAT_EN VDD 0.01034f
C151 dffsnq_0/a_2364_282# RSTn 0
C152 or2_0/a_n505_n1653# VDD 0.02363f
C153 REC_EN dffrnq_0/a_3043_n1702# 0
C154 dffsnq_0/a_1179_653# m2_3305_n910# 0.00217f
C155 dffrnq_0/a_450_n2119# dffsnq_0/a_1492_238# 0
C156 dffrnq_0/a_2250_n1702# VDD 0.00121f
C157 dffsnq_0/a_3268_233# dffrnq_0/a_2250_n1702# 0.00269f
C158 MODE REC_EN 0.02483f
C159 dffrnq_0/a_1458_n1702# REC_EN 0
C160 dffrnq_0/a_38_n1706# m2_3305_n910# 0
C161 dffsnq_0/a_587_598# REC_EN 0.02152f
C162 S0 nor2_0/a_1490_n1804# 0
C163 dffsnq_0/a_175_277# m2_3305_n910# 0.18381f
C164 dffsnq_0/a_1492_238# dffrnq_0/a_1310_n2146# 0.00298f
C165 dffrnq_0/a_1206_n2102# VDD 0
C166 S0 VSS 1.59025f
C167 m2_3239_n1773# VSS 0.34956f
C168 m2_3305_n910# VSS 0.42172f
C169 REC_EN VSS 2.59992f
C170 and2_0/a_3366_935# VSS 0.39003f
C171 RSTn VSS 2.29321f
C172 CLK VSS 0.85504f
C173 dffrnq_0/a_1206_n2102# VSS 0.01297f
C174 dffrnq_0/a_2562_n1702# VSS 0.01697f
C175 dffrnq_0/a_2250_n1702# VSS 0.37403f
C176 dffrnq_0/a_2667_n1842# VSS 0.62674f
C177 dffrnq_0/a_1002_n2102# VSS 0.29173f
C178 dffrnq_0/a_798_n2102# VSS 0.02321f
C179 dffrnq_0/a_1310_n2146# VSS 0.28051f
C180 dffrnq_0/a_450_n2119# VSS 0.68629f
C181 dffrnq_0/a_38_n1706# VSS 1.44454f
C182 TREAT_EN VSS 0.05875f
C183 MODE VSS 0.88592f
C184 or2_0/a_n505_n1653# VSS 0.35258f
C185 VDD VSS 21.66842f
C186 dffsnq_0/a_2588_282# VSS 0.04999f
C187 dffsnq_0/a_2364_282# VSS 0.43821f
C188 dffsnq_0/a_3268_233# VSS 0.59174f
C189 dffsnq_0/a_975_282# VSS 0.01977f
C190 dffsnq_0/a_1179_653# VSS 0.3045f
C191 dffsnq_0/a_1492_238# VSS 0.28879f
C192 dffsnq_0/a_587_598# VSS 1.23015f
C193 dffsnq_0/a_175_277# VSS 1.33067f
.ends

X1 MODE RSTn vss CLK vdd TREAT_EN REC_EN FSM2
.ic v(rec_en)=5 v(x1.s0)=0




.control
save all
**
let vhi      = 5
let fclk     = 1e5
let tper_clk = 1/fclk
let tfr_clk  = 0.01*tper_clk
let ton_clk  = 0.5*tper_clk - 2*tfr_clk
let tper2clk = 0.95*tper_clk
let tmax     = tfr_clk/200
let tstep    = tmax
let tstop    = 8*tper_clk
let tfr      = tfr_clk
**
** CLK: first rising edge at 1.5 clock periods, so the
** forced state holds for a while before anything captures
let td_clk = 1.5*tper_clk
alter @v4[PULSE] = [ 0 $&vhi $&td_clk $&tfr_clk $&tfr_clk $&ton_clk $&tper2clk 0 ]
**
** MODE: held LOW for this run
alter @v3[PULSE] = [ 5 5 5 $&tfr $&tfr $&tstop $&tstop 0 ]
**
** RSTn: held HIGH the whole run so reset never forces a state
alter @v5[PULSE] = [ $&vhi $&vhi 0 $&tfr $&tfr $&tstop $&tstop 0 ]
**
tran $&tstep $&tstop 0 $&tmax uic
**
plot v(clk) v(rstn)+7 v(x1.s0)+14 v(rec_en)+21 v(treat_en)+28
wrdata /foss/designs/DBSchip/FSM2/sim/fsm2_state10_5v0_mode1.txt v(clk) v(mode) v(rstn) v(x1.s0)
+ v(rec_en) v(treat_en)
.endc


**** end user architecture code
**.ends
.GLOBAL GND
.end
